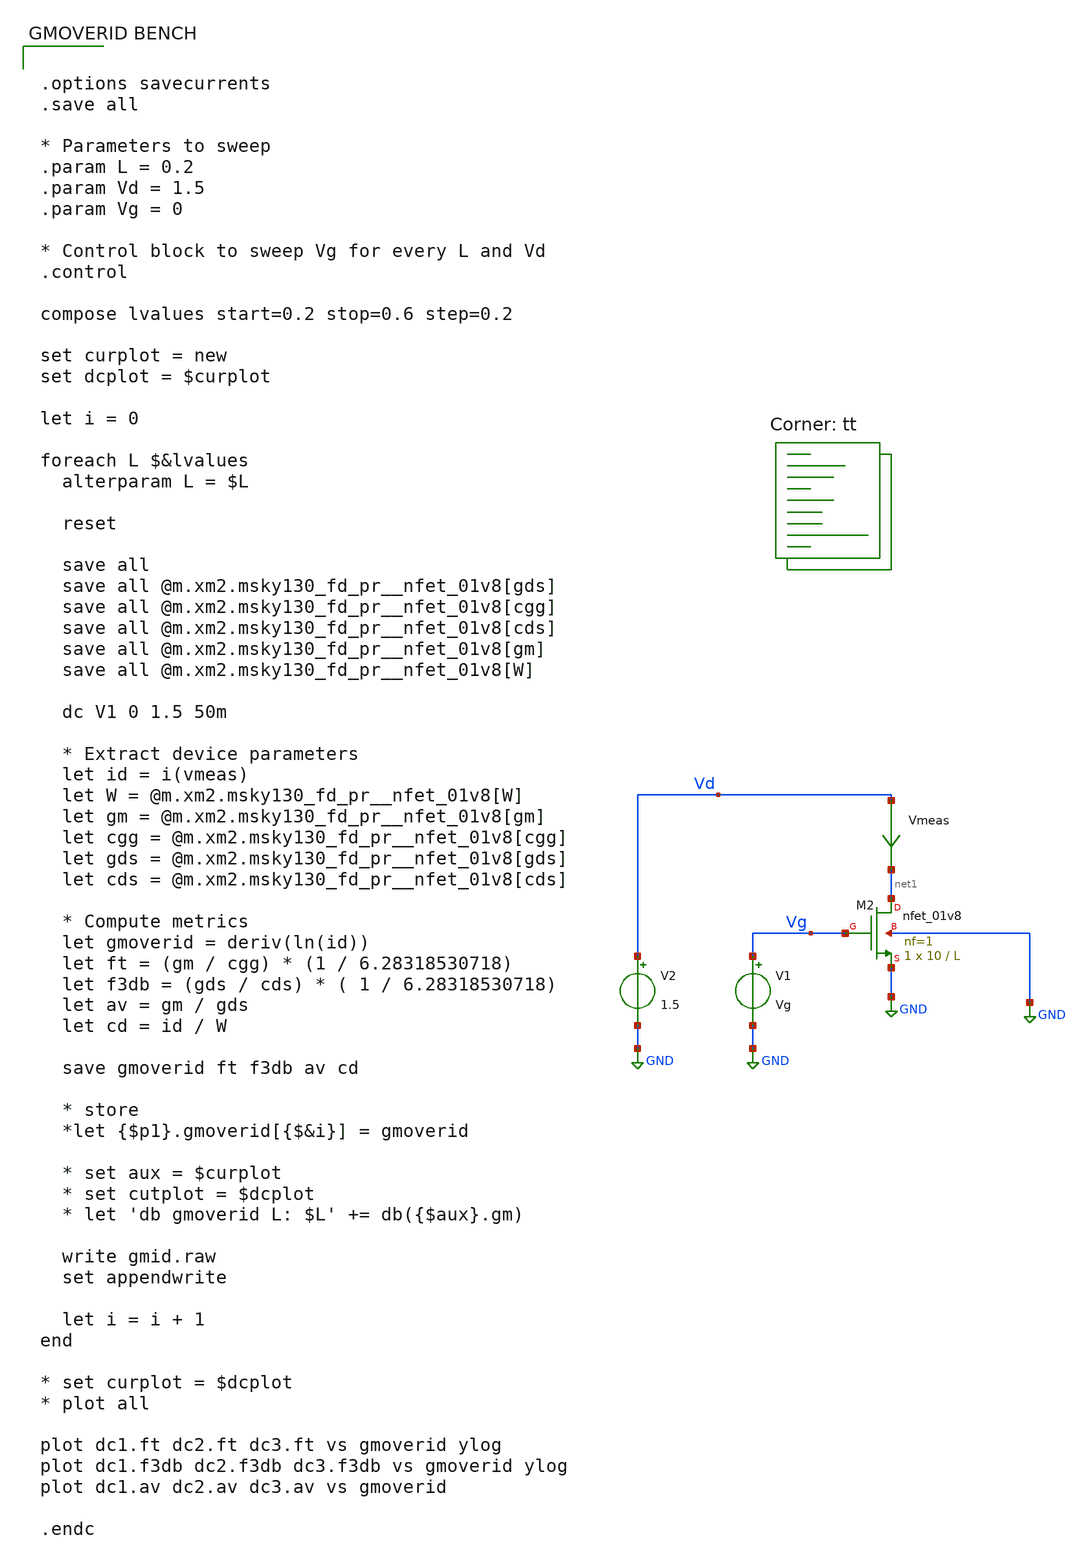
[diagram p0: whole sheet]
** sch_path: gmid.sch
**.subckt gmid
V1 Vg GND Vg
V2 Vd GND 1.5
XM2 net1 Vg GND GND sky130_fd_pr__nfet_01v8 L=L W=10 nf=1 ad='int((1 + 1)/2) * 10 / 1 * 0.29' as='int((1 + 2)/2) * 10 / 1 * 0.29'
+ pd='2*int((1 + 1)/2) * (10 / 1 + 0.29)' ps='2*int((1 + 2)/2) * (10 / 1 + 0.29)' nrd='0.29 / 10 ' nrs='0.29 / 10 '
+ sa=0 sb=0 sd=0 mult=1 m=1
Vmeas Vd net1 0
.save i(vmeas)
**** begin user architecture code
.lib $::SKYWATER_MODELS/sky130.lib.spice tt


.options savecurrents
.save all

* Parameters to sweep
.param L = 0.2
.param Vd = 1.5
.param Vg = 0

* Control block to sweep Vg for every L and Vd
.control

compose lvalues start=0.2 stop=0.6 step=0.2

set curplot = new
set dcplot = $curplot

let i = 0

foreach L $&lvalues
  alterparam L = $L

  reset

  save all
  save all @m.xm2.msky130_fd_pr__nfet_01v8[gds]
  save all @m.xm2.msky130_fd_pr__nfet_01v8[cgg]
  save all @m.xm2.msky130_fd_pr__nfet_01v8[cds]
  save all @m.xm2.msky130_fd_pr__nfet_01v8[gm]
  save all @m.xm2.msky130_fd_pr__nfet_01v8[W]

  dc V1 0 1.5 50m

  * Extract device parameters
  let id = i(vmeas)
  let W = @m.xm2.msky130_fd_pr__nfet_01v8[W]
  let gm = @m.xm2.msky130_fd_pr__nfet_01v8[gm]
  let cgg = @m.xm2.msky130_fd_pr__nfet_01v8[cgg]
  let gds = @m.xm2.msky130_fd_pr__nfet_01v8[gds]
  let cds = @m.xm2.msky130_fd_pr__nfet_01v8[cds]

  * Compute metrics
  let gmoverid = deriv(ln(id))
  let ft = (gm / cgg) * (1 / 6.28318530718)
  let f3db = (gds / cds) * ( 1 / 6.28318530718)
  let av = gm / gds
  let cd = id / W

  save gmoverid ft f3db av cd

  * store
  *let {$p1}.gmoverid[{$&i}] = gmoverid

  * set aux = $curplot
  * set cutplot = $dcplot
  * let 'db gmoverid L: $L' += db({$aux}.gm)

  write gmid.raw
  set appendwrite

  let i = i + 1
end

* set curplot = $dcplot
* plot all

plot dc1.ft dc2.ft dc3.ft vs gmoverid ylog
plot dc1.f3db dc2.f3db dc3.f3db vs gmoverid ylog
plot dc1.av dc2.av dc3.av vs gmoverid

.endc


**** end user architecture code
**.ends
.GLOBAL GND
.end
